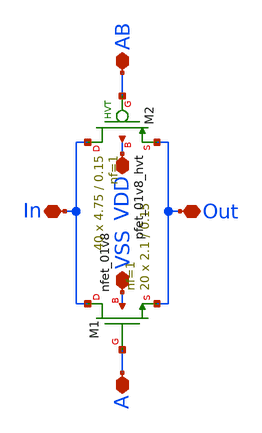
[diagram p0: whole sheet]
** sch_path: HVT/load_x10/load_x10.sch
**.subckt load_x10 In Out VDD VSS AB A
*.iopin In
*.iopin Out
*.iopin VDD
*.iopin VSS
*.iopin AB
*.iopin A
XM1 In A Out VSS sky130_fd_pr__nfet_01v8 L=0.15 W=2.1 nf=1 ad='int((nf+1)/2) * W/nf * 0.29' as='int((nf+2)/2) * W/nf * 0.29'
+ pd='2*int((nf+1)/2) * (W/nf + 0.29)' ps='2*int((nf+2)/2) * (W/nf + 0.29)' nrd='0.29 / W' nrs='0.29 / W'
+ sa=0 sb=0 sd=0 mult=20 m=20
XM2 In AB Out VDD sky130_fd_pr__pfet_01v8_hvt L=0.15 W=4.75 nf=1 ad='int((nf+1)/2) * W/nf * 0.29' as='int((nf+2)/2) * W/nf * 0.29'
+ pd='2*int((nf+1)/2) * (W/nf + 0.29)' ps='2*int((nf+2)/2) * (W/nf + 0.29)' nrd='0.29 / W' nrs='0.29 / W'
+ sa=0 sb=0 sd=0 mult=40 m=40
**.ends
.end
